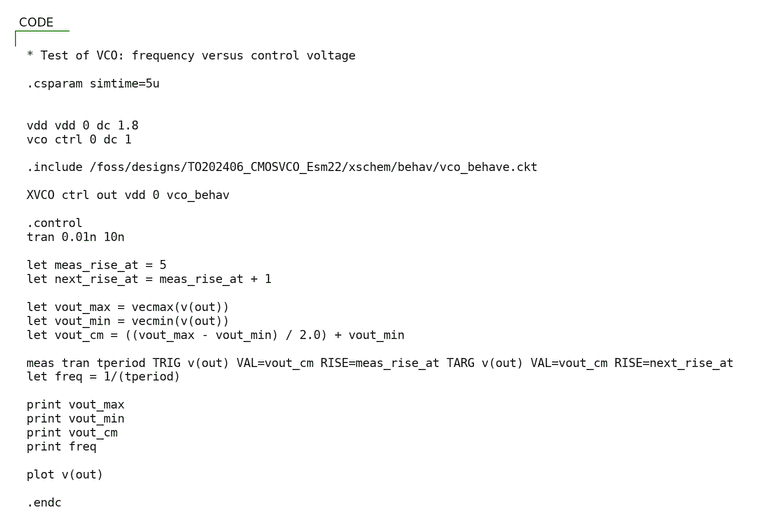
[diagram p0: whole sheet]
** sch_path: xschem/behav/tb_vco_behave_jm_v1p1.sch
**.subckt tb_vco_behave_jm_v1p1
**** begin user architecture code


* Test of VCO: frequency versus control voltage

.csparam simtime=5u


vdd vdd 0 dc 1.8
vco ctrl 0 dc 1

.include /foss/designs/TO202406_CMOSVCO_Esm22/xschem/behav/vco_behave.ckt

XVCO ctrl out vdd 0 vco_behav

.control
tran 0.01n 10n

let meas_rise_at = 5
let next_rise_at = meas_rise_at + 1

let vout_max = vecmax(v(out))
let vout_min = vecmin(v(out))
let vout_cm = ((vout_max - vout_min) / 2.0) + vout_min

meas tran tperiod TRIG v(out) VAL=vout_cm RISE=meas_rise_at TARG v(out) VAL=vout_cm
+ RISE=next_rise_at
let freq = 1/(tperiod)

print vout_max
print vout_min
print vout_cm
print freq

plot v(out)

.endc




**** end user architecture code
**.ends
.end
